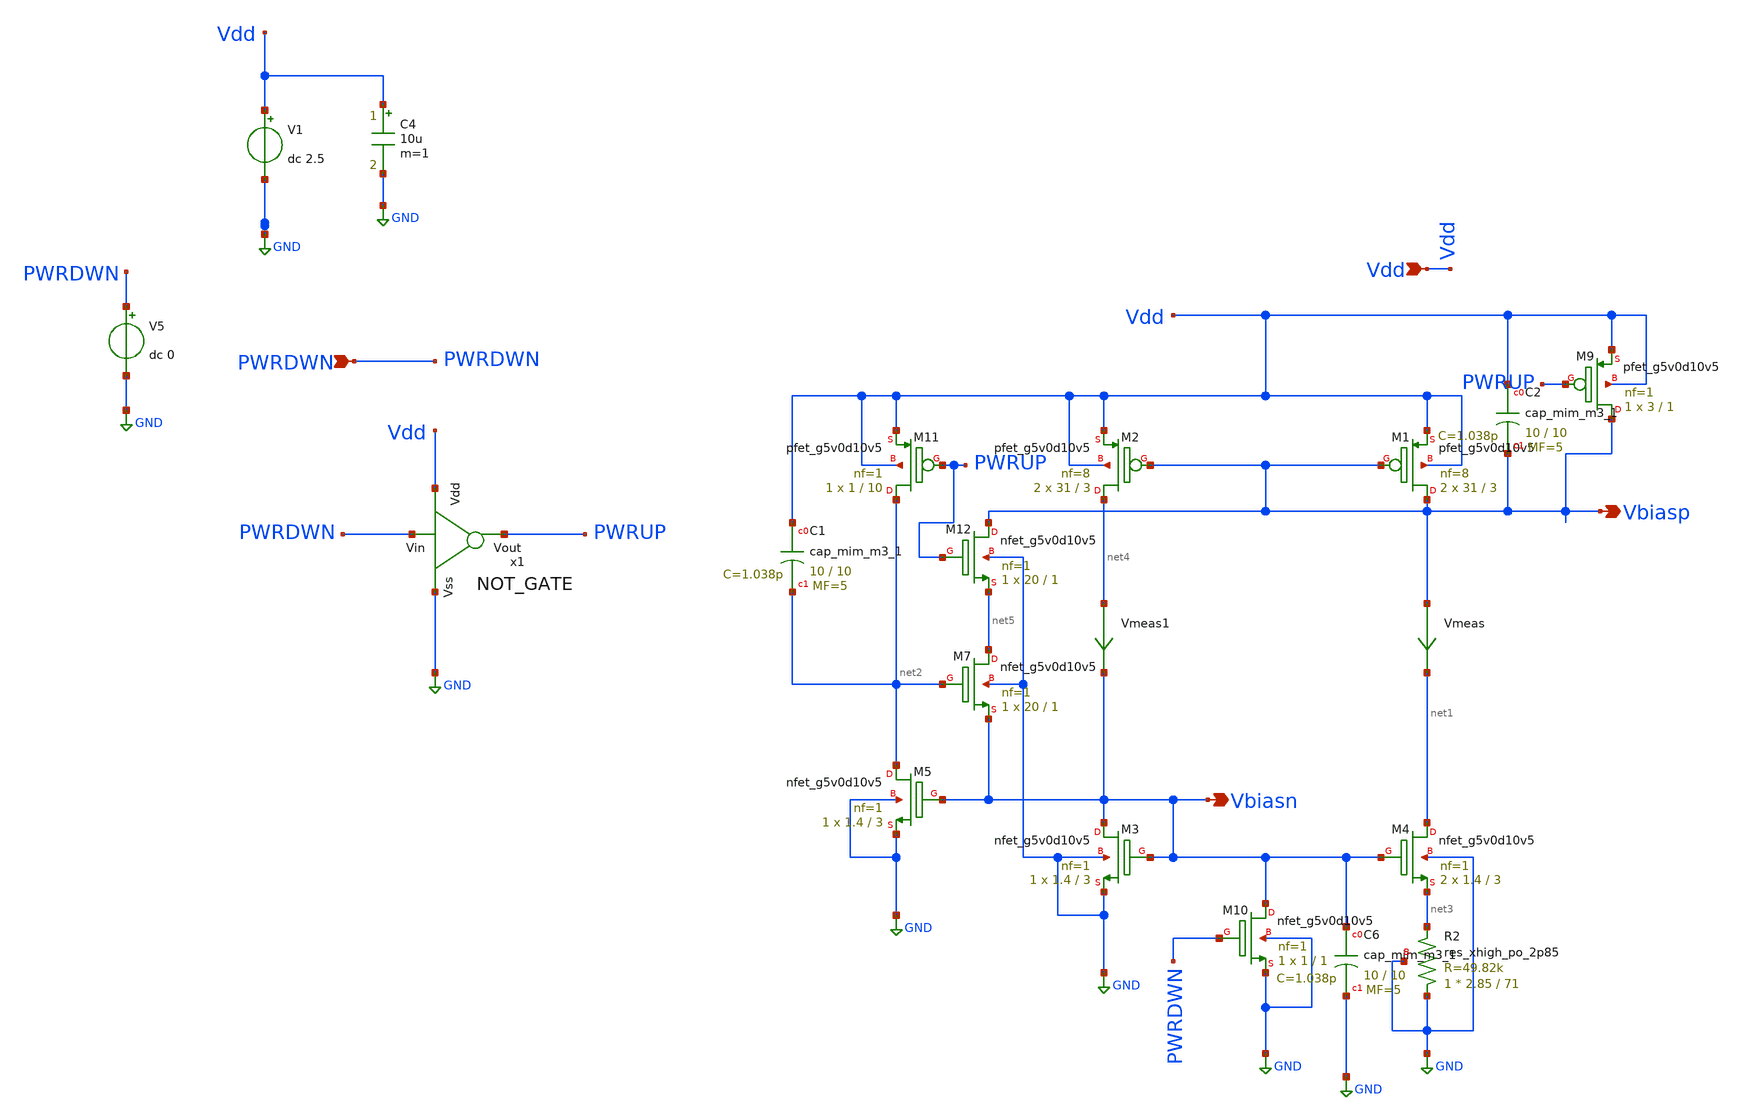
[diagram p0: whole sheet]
** sch_path: xschem/BMR_TB.sch
**.subckt BMR_TB Vdd Vbiasn Vbiasp PWRDWN
*.ipin Vdd
*.opin Vbiasn
*.opin Vbiasp
*.ipin PWRDWN
V1 Vdd GND dc 2.5
V5 PWRDWN GND dc 0
C4 Vdd GND 10u m=1
XM3 Vbiasn Vbiasn GND GND sky130_fd_pr__nfet_g5v0d10v5 L=3 W=1.4 nf=1 ad='int((1 + 1)/2) * 1.4 / 1 * 0.29'
+ as='int((1 + 2)/2) * 1.4 / 1 * 0.29' pd='2*int((1 + 1)/2) * (1.4 / 1 + 0.29)' ps='2*int((1 + 2)/2) * (1.4 / 1 + 0.29)'
+ nrd='0.29 / 1.4 ' nrs='0.29 / 1.4 ' sa=0 sb=0 sd=0 mult=1 m=1
XM1 Vbiasp Vbiasp Vdd Vdd sky130_fd_pr__pfet_g5v0d10v5 L=3 W=31 nf=8 ad='int((8 + 1)/2) * 31 / 8 * 0.29'
+ as='int((8 + 2)/2) * 31 / 8 * 0.29' pd='2*int((8 + 1)/2) * (31 / 8 + 0.29)' ps='2*int((8 + 2)/2) * (31 / 8 + 0.29)'
+ nrd='0.29 / 31 ' nrs='0.29 / 31 ' sa=0 sb=0 sd=0 mult=2 m=2
XM2 net4 Vbiasp Vdd Vdd sky130_fd_pr__pfet_g5v0d10v5 L=3 W=31 nf=8 ad='int((8 + 1)/2) * 31 / 8 * 0.29'
+ as='int((8 + 2)/2) * 31 / 8 * 0.29' pd='2*int((8 + 1)/2) * (31 / 8 + 0.29)' ps='2*int((8 + 2)/2) * (31 / 8 + 0.29)'
+ nrd='0.29 / 31 ' nrs='0.29 / 31 ' sa=0 sb=0 sd=0 mult=2 m=2
XM11 net2 PWRUP Vdd Vdd sky130_fd_pr__pfet_g5v0d10v5 L=10 W=1 nf=1 ad='int((1 + 1)/2) * 1 / 1 * 0.29'
+ as='int((1 + 2)/2) * 1 / 1 * 0.29' pd='2*int((1 + 1)/2) * (1 / 1 + 0.29)' ps='2*int((1 + 2)/2) * (1 / 1 + 0.29)'
+ nrd='0.29 / 1 ' nrs='0.29 / 1 ' sa=0 sb=0 sd=0 mult=1 m=1
XM4 net1 Vbiasn net3 GND sky130_fd_pr__nfet_g5v0d10v5 L=3 W=1.4 nf=1 ad='int((1 + 1)/2) * 1.4 / 1 * 0.29'
+ as='int((1 + 2)/2) * 1.4 / 1 * 0.29' pd='2*int((1 + 1)/2) * (1.4 / 1 + 0.29)' ps='2*int((1 + 2)/2) * (1.4 / 1 + 0.29)'
+ nrd='0.29 / 1.4 ' nrs='0.29 / 1.4 ' sa=0 sb=0 sd=0 mult=2 m=2
XM5 net2 Vbiasn GND GND sky130_fd_pr__nfet_g5v0d10v5 L=3 W=1.4 nf=1 ad='int((1 + 1)/2) * 1.4 / 1 * 0.29'
+ as='int((1 + 2)/2) * 1.4 / 1 * 0.29' pd='2*int((1 + 1)/2) * (1.4 / 1 + 0.29)' ps='2*int((1 + 2)/2) * (1.4 / 1 + 0.29)'
+ nrd='0.29 / 1.4 ' nrs='0.29 / 1.4 ' sa=0 sb=0 sd=0 mult=1 m=1
XM7 net5 net2 Vbiasn GND sky130_fd_pr__nfet_g5v0d10v5 L=1 W=20 nf=1 ad='int((1 + 1)/2) * 20 / 1 * 0.29'
+ as='int((1 + 2)/2) * 20 / 1 * 0.29' pd='2*int((1 + 1)/2) * (20 / 1 + 0.29)' ps='2*int((1 + 2)/2) * (20 / 1 + 0.29)'
+ nrd='0.29 / 20 ' nrs='0.29 / 20 ' sa=0 sb=0 sd=0 mult=1 m=1
x1 Vdd PWRUP PWRDWN GND NOT_GATE
XM12 Vbiasp PWRUP net5 GND sky130_fd_pr__nfet_g5v0d10v5 L=1 W=20 nf=1 ad='int((1 + 1)/2) * 20 / 1 * 0.29'
+ as='int((1 + 2)/2) * 20 / 1 * 0.29' pd='2*int((1 + 1)/2) * (20 / 1 + 0.29)' ps='2*int((1 + 2)/2) * (20 / 1 + 0.29)'
+ nrd='0.29 / 20 ' nrs='0.29 / 20 ' sa=0 sb=0 sd=0 mult=1 m=1
XM9 Vbiasp PWRUP Vdd Vdd sky130_fd_pr__pfet_g5v0d10v5 L=1 W=3 nf=1 ad='int((1 + 1)/2) * 3 / 1 * 0.29'
+ as='int((1 + 2)/2) * 3 / 1 * 0.29' pd='2*int((1 + 1)/2) * (3 / 1 + 0.29)' ps='2*int((1 + 2)/2) * (3 / 1 + 0.29)'
+ nrd='0.29 / 3 ' nrs='0.29 / 3 ' sa=0 sb=0 sd=0 mult=1 m=1
XM10 Vbiasn PWRDWN GND GND sky130_fd_pr__nfet_g5v0d10v5 L=1 W=1 nf=1 ad='int((1 + 1)/2) * 1 / 1 * 0.29'
+ as='int((1 + 2)/2) * 1 / 1 * 0.29' pd='2*int((1 + 1)/2) * (1 / 1 + 0.29)' ps='2*int((1 + 2)/2) * (1 / 1 + 0.29)'
+ nrd='0.29 / 1 ' nrs='0.29 / 1 ' sa=0 sb=0 sd=0 mult=1 m=1
Vmeas Vbiasp net1 0
.save i(vmeas)
Vmeas1 net4 Vbiasn 0
.save i(vmeas1)
XC6 Vbiasn GND sky130_fd_pr__cap_mim_m3_1 W=10 L=10 MF=5 m=5
XC1 Vdd net2 sky130_fd_pr__cap_mim_m3_1 W=10 L=10 MF=5 m=5
XC2 Vdd Vbiasp sky130_fd_pr__cap_mim_m3_1 W=10 L=10 MF=5 m=5
XR2 GND net3 GND sky130_fd_pr__res_xhigh_po_2p85 L=71 mult=1 m=1
**** begin user architecture code


.lib /foss/pdks/sky130A/libs.tech/combined/sky130.lib.spice tt_mm

***Centered at 40C and varies to a range of -20 to 100; with 20C being 1-standard dev***
.param TEMPGAUSS = agauss(40, 60, 3)

***Centered at 2.5V and varies to a range of 2V to 3V; with 0.16mV being 1-standard dev***
***param VOLTGAUSS = agauss(2.5, 0.5, 3)

*** Ideal Biasing resistor is 50k with 5% Gold Band Tolerance ***
***param RESGAUSS = agauss(50k, 833.33, 3)

.param ptemp = 'TEMPGAUSS'
***param Vsource = 'VOLTGAUSS'
***param Id_res = 'RESGAUSS'


.options temp = {ptemp}

.csparam ctemp = {ptemp}
***csparam cvolt = {Vsource}
***csparam cres = {Id_res}

.control
 let T = 0
 let V = 0
 let R = 0

let i_count = 100

 let T_vec = vector(i_count)
 *** let V_vec = vector(i_count)
 let R_vec = vector(i_count)

 let IVEC_1 = vector(i_count)
 let IVEC_2 = vector(i_count)

 ***let IVEC_MAX = vector(i_count)
 ***let IVEC_MIN = vector(i_count)

 let index = 0
 option seed = 9
 set wr_vecnames
 dowhile index <= 100
   save all
   save @m.xm4.msky130_fd_pr__nfet_g5v0d10v5[id]

    ***tran 1u 2m
    dc V1 0 5 0.1
    write BMR_MC_TT_POLY_RES_285.raw

   set noprintscale

    meas dc I_1 FIND i(Vmeas) WHEN v(vdd) = 2.5 RISE = 1
    meas dc I_2 FIND i(Vmeas1) WHEN v(vdd) = 2.5 RISE = 1

    let IVEC_1[index] = 'I_1'
    let IVEC_2[index] = 'I_2'

   ***meas tran I_MAX MAX i(Vmeas) FROM = 0.02m TO = 0.48m
   ***meas tran I_MIN MIN i(Vmeas) FROM = 0.52m TO = 0.98m

   ***let IVEC_MAX[index] = 'I_MAX'
   ***let IVEC_MIN[index] = 'I_MIN'

   set appendwrite

   let T = $&ctemp
   let T_vec[index] = 'T'

   ***let V = $&cvolt
   ***let V_vec[index] = 'V'

   let Poly_V = 'v(net3)'
   let Poly_I = @m.xm4.msky130_fd_pr__nfet_g5v0d10v5[id]
   let R = 'Poly_V[25]/Poly_I[25]'
   let R_vec[index] = 'R'

   echo -n This is $&T Celcius
   echo -n This is $&R Ohms
   ***echo -n This is $&V Volts


   reset
   let index = index + 1
  end

  **OL AC
  *** print col GAIN_vec UGW_vec PM_vec T_vec V_vec > FDA_AC_CM_GAIN_UGW_PM_SS_PVT.txt
  **Offset
  ***print col OFFSET_vec T_vec V_vec > FDA_OFFSETS_SS_PVT.txt
  **NOISE
    print col IVEC_1 IVEC_2 T_vec R_vec > BMR_MONTE_CARLO_TT_POLY_RES_285.txt

.endc
.end

**** end user architecture code
**.ends

* expanding   symbol:  NOT_GATE.sym # of pins=4
** sym_path: xschem/NOT_GATE.sym
** sch_path: xschem/NOT_GATE.sch
.subckt NOT_GATE Vdd Vout Vin Vss
*.opin Vout
*.ipin Vdd
*.ipin Vss
*.ipin Vin
XM1 Vout Vin Vss Vss sky130_fd_pr__nfet_g5v0d10v5 L=1 W=1 nf=1 ad='int((1 + 1)/2) * 1 / 1 * 0.29' as='int((1 + 2)/2) * 1 / 1 * 0.29'
+ pd='2*int((1 + 1)/2) * (1 / 1 + 0.29)' ps='2*int((1 + 2)/2) * (1 / 1 + 0.29)' nrd='0.29 / 1 ' nrs='0.29 / 1 '
+ sa=0 sb=0 sd=0 mult=1 m=1
XM2 Vout Vin Vdd Vdd sky130_fd_pr__pfet_g5v0d10v5 L=1 W=3 nf=1 ad='int((1 + 1)/2) * 3 / 1 * 0.29' as='int((1 + 2)/2) * 3 / 1 * 0.29'
+ pd='2*int((1 + 1)/2) * (3 / 1 + 0.29)' ps='2*int((1 + 2)/2) * (3 / 1 + 0.29)' nrd='0.29 / 3 ' nrs='0.29 / 3 '
+ sa=0 sb=0 sd=0 mult=1 m=1
.ends

.GLOBAL GND
.end
